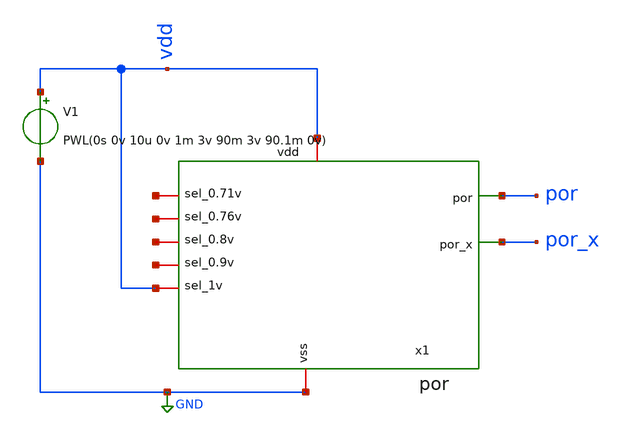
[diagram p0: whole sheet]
** sch_path: 2.schema/tb_POR.sch
**.subckt tb_POR
x1 vdd net1 net2 net3 net4 por vdd por_x GND por
V1 vdd GND PWL(0s 0v 10u 0v 1m 3v 90m 3v 90.1m 0v)
**** begin user architecture code


.tran 1u 100000u


 .include $::LIB/SOI_CMOS
**** end user architecture code
**.ends

* expanding   symbol:  por.sym # of pins=9
** sym_path: 2.schema/por.sym
** sch_path: 2.schema/por.sch
.subckt por vdd sel_0.71v sel_0.76v sel_0.8v sel_0.9v por sel_1v por_x vss
*.iopin vdd
*.iopin vss
*.opin por
*.iopin sel_1v
*.iopin sel_0.9v
*.iopin sel_0.8v
*.iopin sel_0.76v
*.iopin sel_0.71v
*.opin por_x
M1 por net1 net4 net4 pch w=40u l=10u as=0 ps=0 ad=0 pd=0 m=1
M2 por net1 net5 net5 nch w=10u l=10u as=0 ps=0 ad=0 pd=0 m=1
M3 net4 net1 vdd vdd pch w=40u l=10u as=0 ps=0 ad=0 pd=0 m=1
M5 vdd por vdd vdd pch w=40u l=10u as=0 ps=0 ad=0 pd=0 m=2
M6 vdd por net5 net5 nch w=10u l=10u as=0 ps=0 ad=0 pd=0 m=4
M7 net5 net1 vss vss nch w=10u l=10u as=0 ps=0 ad=0 pd=0 m=1
C5 net1 vss 0.413p m=1
C6 net1 vss 0.413p m=1
C7 net1 vss 0.413p m=1
C8 net1 vss 0.413p m=1
RP9 net2 net3 3.6k ac=1k m=1
RP10 net6 net3 3.6k ac=1k m=1
RN11 net1 net6 3.6k ac=1k m=1
M8 net2 net7 vdd vdd pch w=40u l=10u as=0 ps=0 ad=0 pd=0 m=1
RP1 net7 net8 3.6k ac=1k m=1
RN1 sel_0.9v sel_1v 0.54k ac=1k m=1
RN2 sel_0.8v sel_0.9v 0.54k ac=1k m=1
RN3 sel_0.76v sel_0.8v 0.54k ac=1k m=1
RN4 sel_0.71v sel_0.76v 0.54k ac=1k m=1
RN5 sel_1v net7 0.54k ac=1k m=1
RP2 net8 por_x 3.6k ac=1k m=1
M9 por_x por vdd vdd pch w=40u l=10u as=0 ps=0 ad=0 pd=0 m=2
M10 por_x por vss vss nch w=10u l=10u as=0 ps=0 ad=0 pd=0 m=4
M4 net1 vdd vdd vdd pch w=40u l=10u as=0 ps=0 ad=0 pd=0 m=1
.ends

.GLOBAL GND
.end
